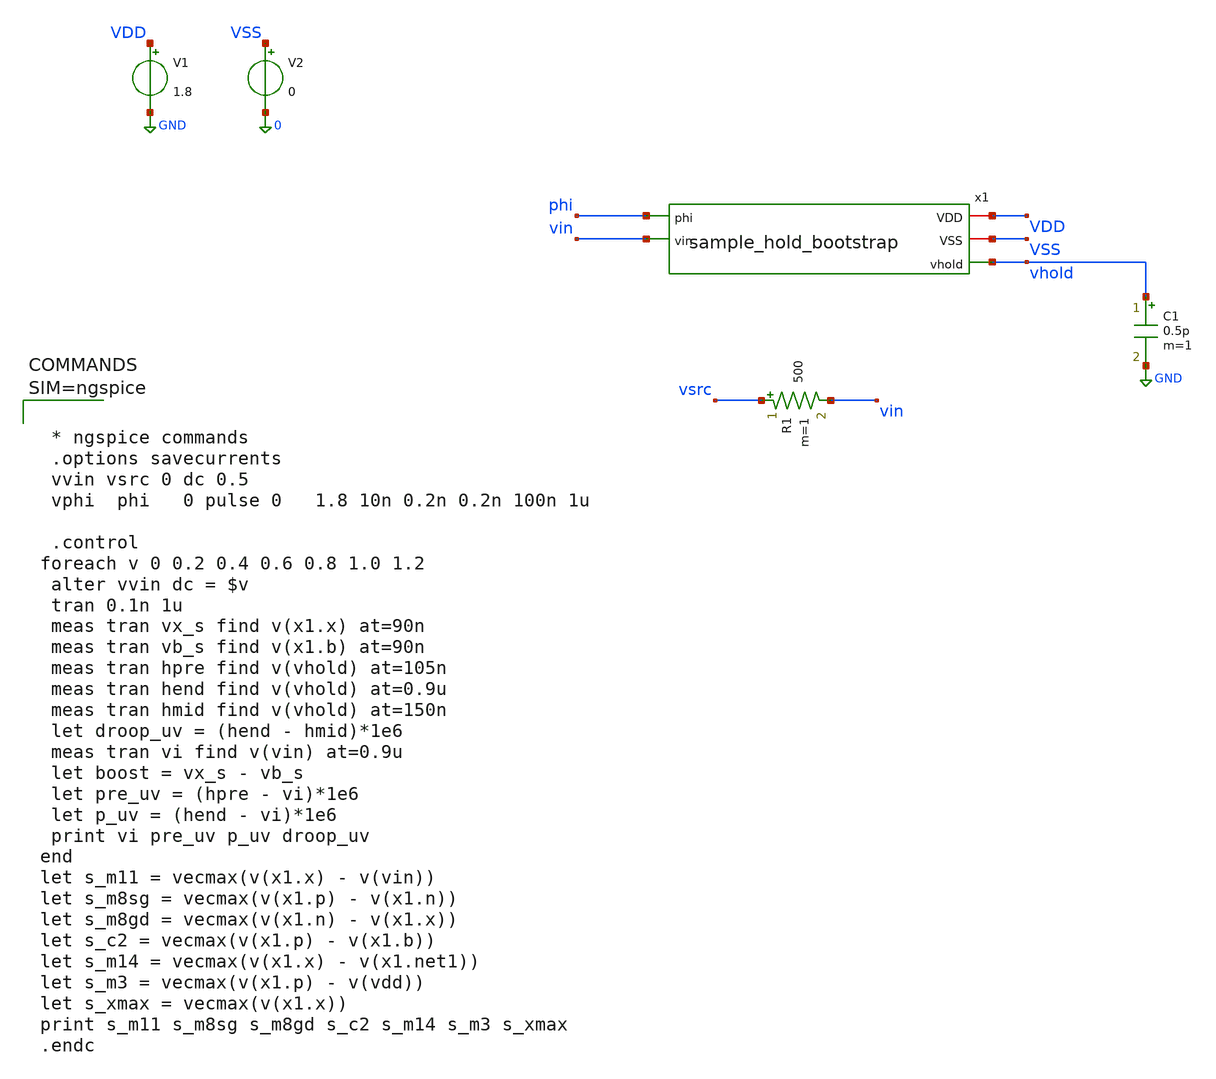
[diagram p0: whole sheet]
** sch_path: xschem/sample_hold_bootstrap_tb.sch
**.subckt sample_hold_bootstrap_tb
V1 VDD GND 1.8
V2 VSS 0 0
x1 phi VDD VSS vin vhold sample_hold_bootstrap
R1 vsrc vin 500 m=1
C1 vhold GND 0.5p m=1
**** begin user architecture code

** opencircuitdesign pdks install
.lib $::SKYWATER_MODELS/sky130.lib.spice tt




 * ngspice commands
 .options savecurrents
 vvin vsrc 0 dc 0.5
 vphi  phi   0 pulse 0   1.8 10n 0.2n 0.2n 100n 1u

 .control
foreach v 0 0.2 0.4 0.6 0.8 1.0 1.2
 alter vvin dc = $v
 tran 0.1n 1u
 meas tran vx_s find v(x1.x) at=90n
 meas tran vb_s find v(x1.b) at=90n
 meas tran hpre find v(vhold) at=105n
 meas tran hend find v(vhold) at=0.9u
 meas tran hmid find v(vhold) at=150n
 let droop_uv = (hend - hmid)*1e6
 meas tran vi find v(vin) at=0.9u
 let boost = vx_s - vb_s
 let pre_uv = (hpre - vi)*1e6
 let p_uv = (hend - vi)*1e6
 print vi pre_uv p_uv droop_uv
end
let s_m11 = vecmax(v(x1.x) - v(vin))
let s_m8sg = vecmax(v(x1.p) - v(x1.n))
let s_m8gd = vecmax(v(x1.n) - v(x1.x))
let s_c2 = vecmax(v(x1.p) - v(x1.b))
let s_m14 = vecmax(v(x1.x) - v(x1.net1))
let s_m3 = vecmax(v(x1.p) - v(vdd))
let s_xmax = vecmax(v(x1.x))
print s_m11 s_m8sg s_m8gd s_c2 s_m14 s_m3 s_xmax
.endc



**** end user architecture code
**.ends

* expanding   symbol:  sample_hold_bootstrap.sym # of pins=5
** sym_path: xschem/sample_hold_bootstrap.sym
** sch_path: xschem/sample_hold_bootstrap.sch
.subckt sample_hold_bootstrap phi VDD VSS vin vhold
*.iopin VDD
*.iopin VSS
*.opin vhold
*.ipin phi
*.ipin vin
XM8 X N P P sky130_fd_pr__pfet_01v8 L=0.15 W=2 nf=1 ad='int((1 + 1)/2) * 2 / 1 * 0.29' as='int((1 + 2)/2) * 2 / 1 * 0.29'
+ pd='2*int((1 + 1)/2) * (2 / 1 + 0.29)' ps='2*int((1 + 2)/2) * (2 / 1 + 0.29)' nrd='0.29 / 2 ' nrs='0.29 / 2 '
+ sa=0 sb=0 sd=0 mult=1 m=1
XM11 vin X vhold VSS sky130_fd_pr__nfet_01v8 L=0.15 W=1 nf=1 ad='int((1 + 1)/2) * 1 / 1 * 0.29' as='int((1 + 2)/2) * 1 / 1 * 0.29'
+ pd='2*int((1 + 1)/2) * (1 / 1 + 0.29)' ps='2*int((1 + 2)/2) * (1 / 1 + 0.29)' nrd='0.29 / 1 ' nrs='0.29 / 1 '
+ sa=0 sb=0 sd=0 mult=1 m=1
XC1 vhold VSS sky130_fd_pr__cap_mim_m3_1 W=22 L=22 MF=2 m=2
XC2 P B sky130_fd_pr__cap_mim_m3_1 W=11 L=11 MF=2 m=2
XM9 B X vin VSS sky130_fd_pr__nfet_01v8 L=0.15 W=2 nf=1 ad='int((1 + 1)/2) * 2 / 1 * 0.29' as='int((1 + 2)/2) * 2 / 1 * 0.29'
+ pd='2*int((1 + 1)/2) * (2 / 1 + 0.29)' ps='2*int((1 + 2)/2) * (2 / 1 + 0.29)' nrd='0.29 / 2 ' nrs='0.29 / 2 '
+ sa=0 sb=0 sd=0 mult=1 m=1
XM12 VSS phi_b B VSS sky130_fd_pr__nfet_01v8 L=0.15 W=1 nf=1 ad='int((1 + 1)/2) * 1 / 1 * 0.29' as='int((1 + 2)/2) * 1 / 1 * 0.29'
+ pd='2*int((1 + 1)/2) * (1 / 1 + 0.29)' ps='2*int((1 + 2)/2) * (1 / 1 + 0.29)' nrd='0.29 / 1 ' nrs='0.29 / 1 '
+ sa=0 sb=0 sd=0 mult=1 m=1
XM14 X VDD net1 VSS sky130_fd_pr__nfet_01v8 L=0.15 W=1 nf=1 ad='int((1 + 1)/2) * 1 / 1 * 0.29' as='int((1 + 2)/2) * 1 / 1 * 0.29'
+ pd='2*int((1 + 1)/2) * (1 / 1 + 0.29)' ps='2*int((1 + 2)/2) * (1 / 1 + 0.29)' nrd='0.29 / 1 ' nrs='0.29 / 1 '
+ sa=0 sb=0 sd=0 mult=1 m=1
XM3 P X VDD P sky130_fd_pr__pfet_01v8 L=0.15 W=2 nf=1 ad='int((1 + 1)/2) * 2 / 1 * 0.29' as='int((1 + 2)/2) * 2 / 1 * 0.29'
+ pd='2*int((1 + 1)/2) * (2 / 1 + 0.29)' ps='2*int((1 + 2)/2) * (2 / 1 + 0.29)' nrd='0.29 / 2 ' nrs='0.29 / 2 '
+ sa=0 sb=0 sd=0 mult=1 m=1
XM10 net1 phi_b VSS VSS sky130_fd_pr__nfet_01v8 L=0.15 W=1 nf=1 ad='int((1 + 1)/2) * 1 / 1 * 0.29' as='int((1 + 2)/2) * 1 / 1 * 0.29'
+ pd='2*int((1 + 1)/2) * (1 / 1 + 0.29)' ps='2*int((1 + 2)/2) * (1 / 1 + 0.29)' nrd='0.29 / 1 ' nrs='0.29 / 1 '
+ sa=0 sb=0 sd=0 mult=1 m=1
XM15 N phi B VSS sky130_fd_pr__nfet_01v8 L=0.15 W=1 nf=1 ad='int((1 + 1)/2) * 1 / 1 * 0.29' as='int((1 + 2)/2) * 1 / 1 * 0.29'
+ pd='2*int((1 + 1)/2) * (1 / 1 + 0.29)' ps='2*int((1 + 2)/2) * (1 / 1 + 0.29)' nrd='0.29 / 1 ' nrs='0.29 / 1 '
+ sa=0 sb=0 sd=0 mult=1 m=1
XM16 N phi VDD VDD sky130_fd_pr__pfet_01v8 L=0.15 W=1 nf=1 ad='int((1 + 1)/2) * 1 / 1 * 0.29' as='int((1 + 2)/2) * 1 / 1 * 0.29'
+ pd='2*int((1 + 1)/2) * (1 / 1 + 0.29)' ps='2*int((1 + 2)/2) * (1 / 1 + 0.29)' nrd='0.29 / 1 ' nrs='0.29 / 1 '
+ sa=0 sb=0 sd=0 mult=1 m=1
XMIN phi_b phi VSS VSS sky130_fd_pr__nfet_01v8 L=0.15 W=1 nf=1 ad='int((1 + 1)/2) * 1 / 1 * 0.29' as='int((1 + 2)/2) * 1 / 1 * 0.29'
+ pd='2*int((1 + 1)/2) * (1 / 1 + 0.29)' ps='2*int((1 + 2)/2) * (1 / 1 + 0.29)' nrd='0.29 / 1 ' nrs='0.29 / 1 '
+ sa=0 sb=0 sd=0 mult=1 m=1
XMIP phi_b phi VDD VDD sky130_fd_pr__pfet_01v8 L=0.15 W=2 nf=1 ad='int((1 + 1)/2) * 2 / 1 * 0.29' as='int((1 + 2)/2) * 2 / 1 * 0.29'
+ pd='2*int((1 + 1)/2) * (2 / 1 + 0.29)' ps='2*int((1 + 2)/2) * (2 / 1 + 0.29)' nrd='0.29 / 2 ' nrs='0.29 / 2 '
+ sa=0 sb=0 sd=0 mult=1 m=1
.ends

.GLOBAL GND
.end
